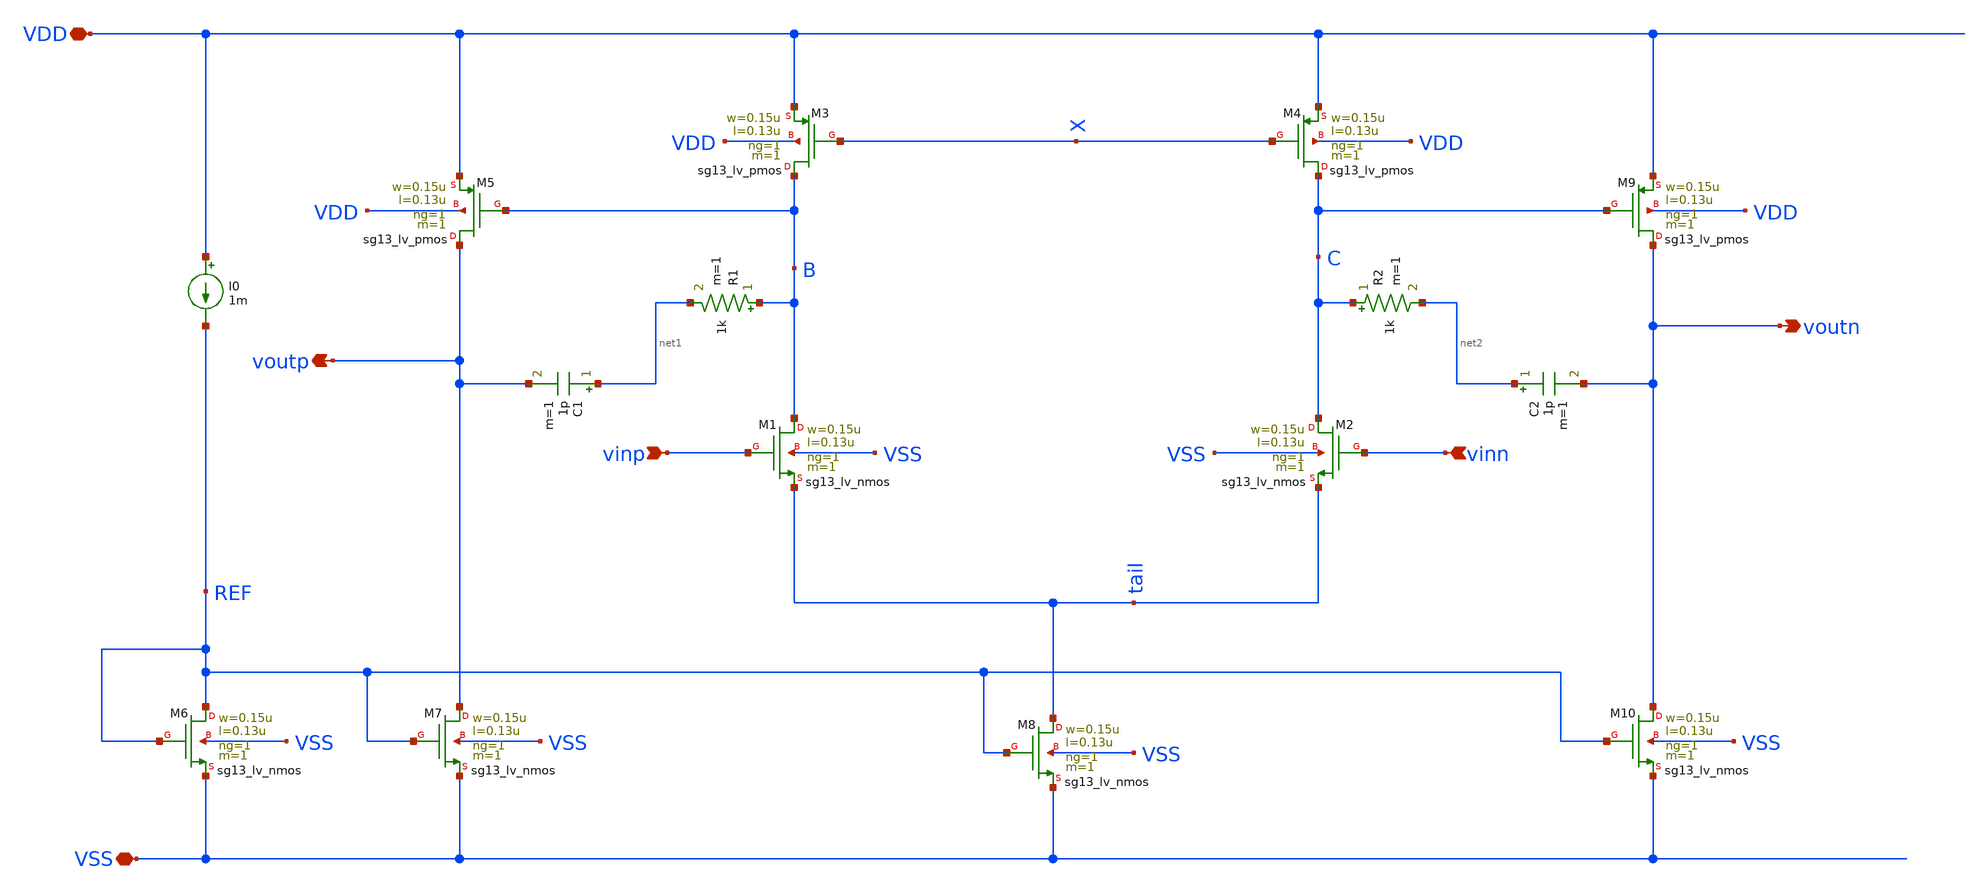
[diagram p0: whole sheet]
** sch_path: analog-db/templates/OTA-Two-Stage/two-stage-miller-comp.sch
**.subckt two-stage-miller-comp vinp vinn voutp voutn VDD VSS
*.ipin vinp
*.ipin vinn
*.opin voutp
*.opin voutn
*.iopin VDD
*.iopin VSS
XM1 B vinp tail VSS sg13_lv_nmos w=0.15u l=0.13u ng=1 m=1 mm_ok=1
XM2 C vinn tail VSS sg13_lv_nmos w=0.15u l=0.13u ng=1 m=1 mm_ok=1
XM3 B X VDD VDD sg13_lv_pmos w=0.15u l=0.13u ng=1 m=1 mm_ok=1
XM4 C X VDD VDD sg13_lv_pmos w=0.15u l=0.13u ng=1 m=1 mm_ok=1
XM5 voutp B VDD VDD sg13_lv_pmos w=0.15u l=0.13u ng=1 m=1 mm_ok=1
XM6 REF REF VSS VSS sg13_lv_nmos w=0.15u l=0.13u ng=1 m=1 mm_ok=1
XM7 voutp REF VSS VSS sg13_lv_nmos w=0.15u l=0.13u ng=1 m=1 mm_ok=1
XM8 tail REF VSS VSS sg13_lv_nmos w=0.15u l=0.13u ng=1 m=1 mm_ok=1
XM9 voutn C VDD VDD sg13_lv_pmos w=0.15u l=0.13u ng=1 m=1 mm_ok=1
XM10 voutn REF VSS VSS sg13_lv_nmos w=0.15u l=0.13u ng=1 m=1 mm_ok=1
I0 VDD REF 1m
R1 B net1 1k m=1
C1 net1 voutp 1p m=1
R2 C net2 1k m=1
C2 net2 voutn 1p m=1
**.ends
.end
